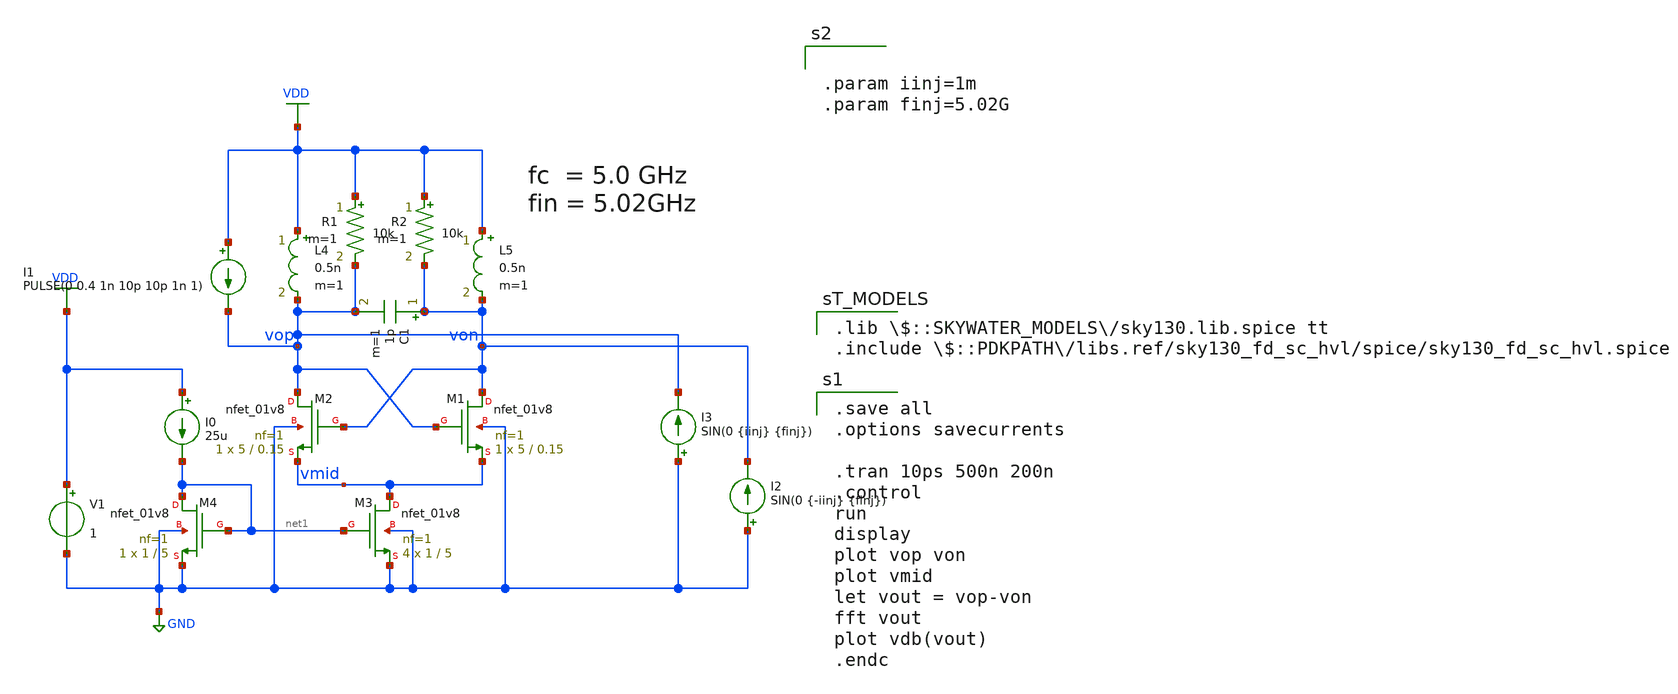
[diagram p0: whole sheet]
** sch_path: SKY130/xschem/injection_locking/XCP_IL_demo.sch
**.subckt XCP_IL_demo
XM1 von vop vmid GND sky130_fd_pr__nfet_01v8 L=0.15 W=5 nf=1 ad='int((nf+1)/2) * W/nf * 0.29' as='int((nf+2)/2) * W/nf * 0.29'
+ pd='2*int((nf+1)/2) * (W/nf + 0.29)' ps='2*int((nf+2)/2) * (W/nf + 0.29)' nrd='0.29 / W' nrs='0.29 / W'
+ sa=0 sb=0 sd=0 mult=1 m=1
XM2 vop von vmid GND sky130_fd_pr__nfet_01v8 L=0.15 W=5 nf=1 ad='int((nf+1)/2) * W/nf * 0.29' as='int((nf+2)/2) * W/nf * 0.29'
+ pd='2*int((nf+1)/2) * (W/nf + 0.29)' ps='2*int((nf+2)/2) * (W/nf + 0.29)' nrd='0.29 / W' nrs='0.29 / W'
+ sa=0 sb=0 sd=0 mult=1 m=1
XM3 vmid net1 GND GND sky130_fd_pr__nfet_01v8 L=5 W=1 nf=1 ad='int((nf+1)/2) * W/nf * 0.29' as='int((nf+2)/2) * W/nf * 0.29'
+ pd='2*int((nf+1)/2) * (W/nf + 0.29)' ps='2*int((nf+2)/2) * (W/nf + 0.29)' nrd='0.29 / W' nrs='0.29 / W'
+ sa=0 sb=0 sd=0 mult=4 m=4
XM4 net1 net1 GND GND sky130_fd_pr__nfet_01v8 L=5 W=1 nf=1 ad='int((nf+1)/2) * W/nf * 0.29' as='int((nf+2)/2) * W/nf * 0.29'
+ pd='2*int((nf+1)/2) * (W/nf + 0.29)' ps='2*int((nf+2)/2) * (W/nf + 0.29)' nrd='0.29 / W' nrs='0.29 / W'
+ sa=0 sb=0 sd=0 mult=1 m=1
V1 VDD GND 1
I0 VDD net1 25u
L4 VDD vop 0.5n m=1
L5 VDD von 0.5n m=1
C1 von vop 1p m=1
I1 VDD vop PULSE(0 0.4 1n 10p 10p 1n 1)
R1 VDD vop 10k m=1
R2 VDD von 10k m=1
I3 GND vop SIN(0 {iinj} {finj})
I2 GND von SIN(0 {-iinj} {finj})
**** begin user architecture code

.save all
.options savecurrents

.tran 10ps 500n 200n
.control
run
display
plot vop von
plot vmid
let vout = vop-von
fft vout
plot vdb(vout)
.endc




.param iinj=1m
.param finj=5.02G



.lib $::SKYWATER_MODELS/sky130.lib.spice tt
.include $::PDKPATH/libs.ref/sky130_fd_sc_hvl/spice/sky130_fd_sc_hvl.spice
**** end user architecture code
**.ends
.GLOBAL GND
.GLOBAL VDD
.end
